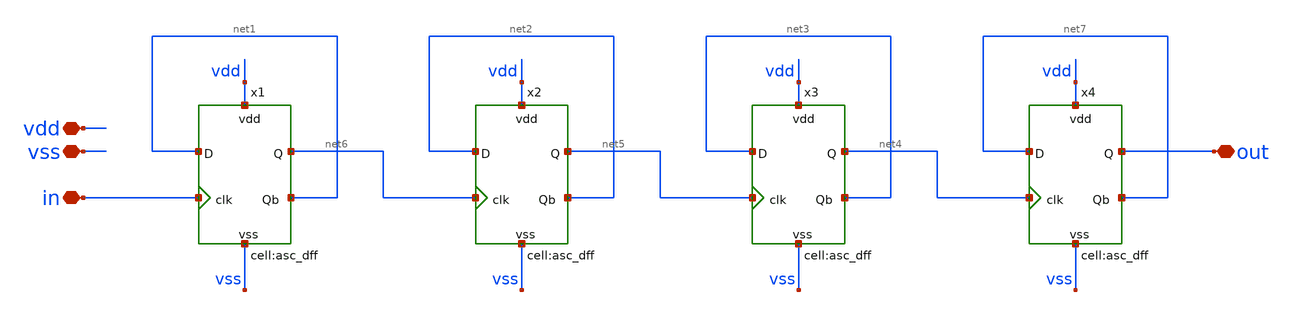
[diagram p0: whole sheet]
** sch_path: designs/libs/xp_core_analog/asc_N_16_divider/asc_N_16_divider.sch
**.subckt asc_N_16_divider vdd vss in out
*.iopin vdd
*.iopin vss
*.iopin in
*.iopin out
x1 in net1 net1 vdd vss net6 asc_dff
x2 net6 net2 net2 vdd vss net5 asc_dff
x3 net5 net3 net3 vdd vss net4 asc_dff
x4 net4 net7 net7 vdd vss out asc_dff
**.ends
.end
